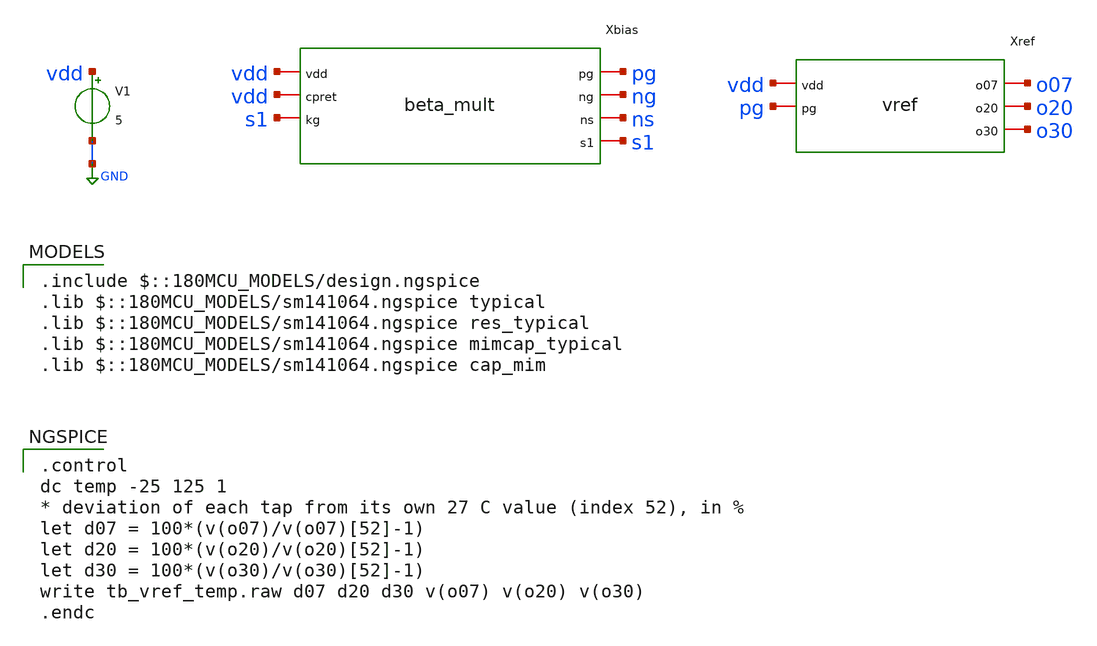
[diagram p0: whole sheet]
** sch_path: Schematics #2/sims/tb/tb_vref_temp.sch
**.subckt tb_vref_temp
V1 vdd GND 5
Xbias vdd pg ng ns vdd s1 s1 beta_mult
Xref vdd pg o07 o20 o30 vref
**** begin user architecture code
 .include $::180MCU_MODELS/design.ngspice
.lib $::180MCU_MODELS/sm141064.ngspice typical
.lib $::180MCU_MODELS/sm141064.ngspice res_typical
.lib $::180MCU_MODELS/sm141064.ngspice mimcap_typical
.lib $::180MCU_MODELS/sm141064.ngspice cap_mim

.control
dc temp -25 125 1
* deviation of each tap from its own 27 C value (index 52), in %
let d07 = 100*(v(o07)/v(o07)[52]-1)
let d20 = 100*(v(o20)/v(o20)[52]-1)
let d30 = 100*(v(o30)/v(o30)[52]-1)
write tb_vref_temp.raw d07 d20 d30 v(o07) v(o20) v(o30)
.endc

**** end user architecture code
**.ends
.GLOBAL GND
.end
